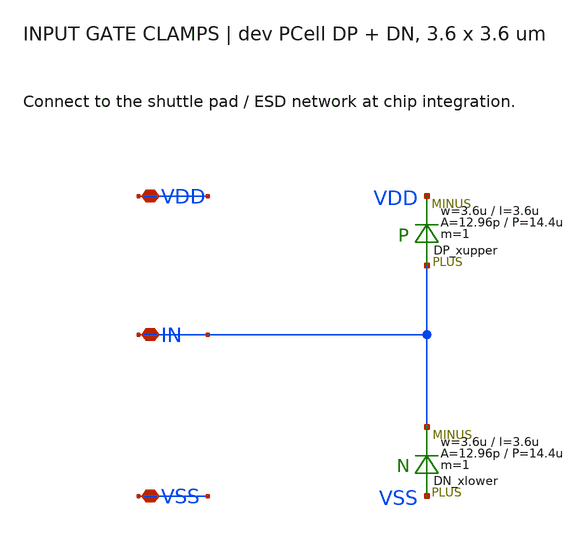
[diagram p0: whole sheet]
** sch_path: member_project/SRAM/PenguinEino/submission/sram512_input_clamp.sch
**.subckt sram512_input_clamp IN VDD VSS
*.iopin IN
*.iopin VDD
*.iopin VSS
Dxupper IN VDD DP m=1
Dxlower VSS IN DN m=1
**.ends
.end
